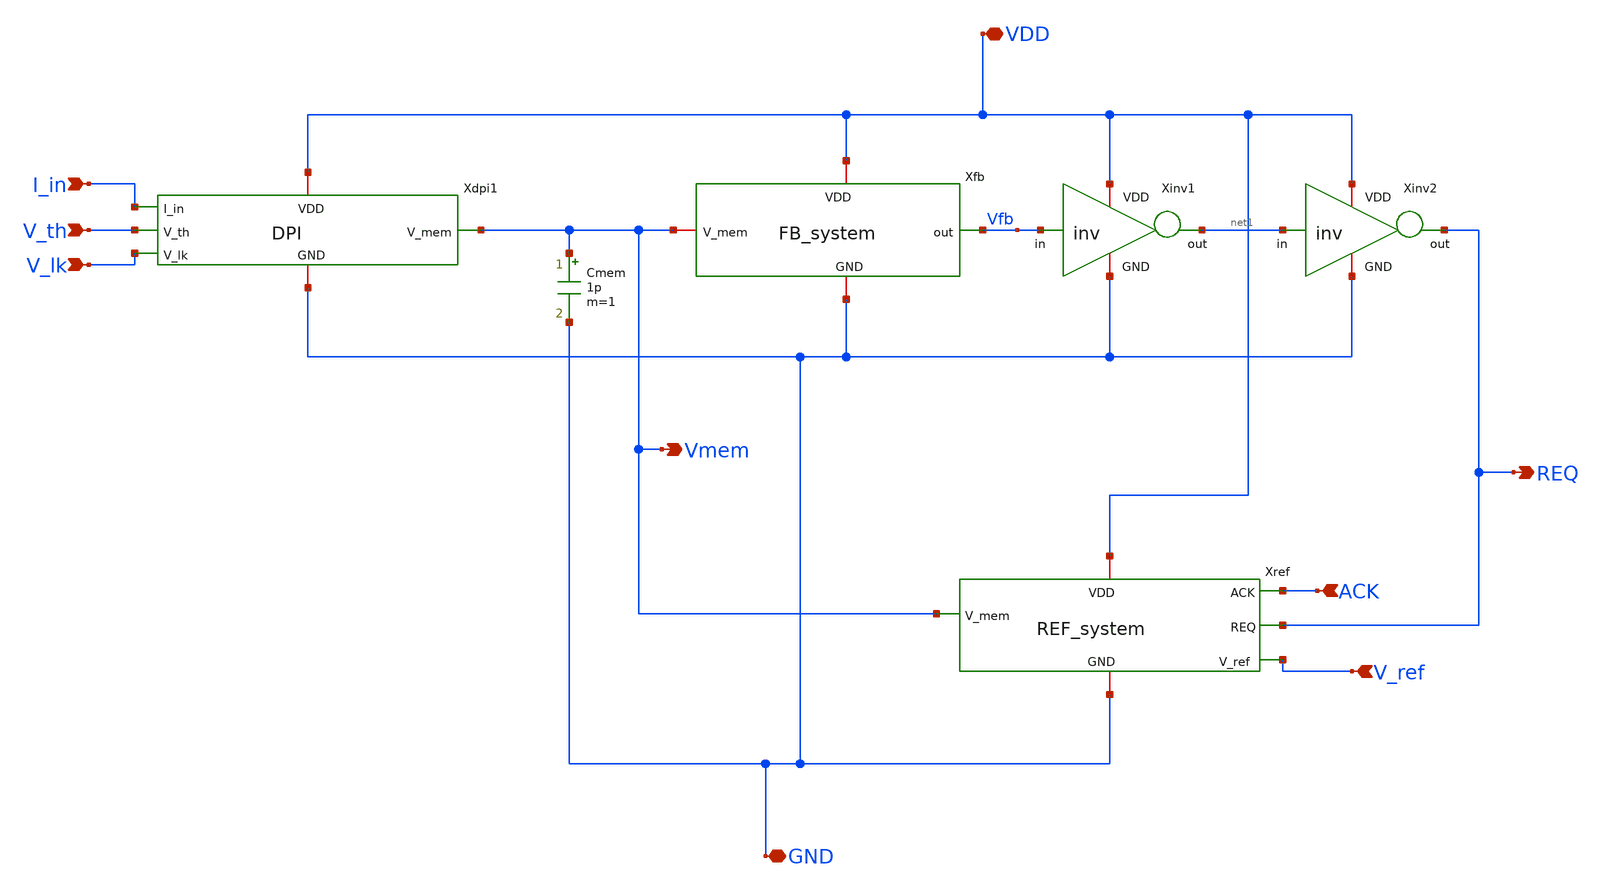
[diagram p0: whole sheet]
** sch_path: xschem/neuron_noahp.sch
**.subckt neuron_noahp V_ref GND VDD REQ ACK I_in V_th V_lk Vmem
*.ipin V_ref
*.iopin GND
*.iopin VDD
*.opin REQ
*.ipin ACK
*.ipin I_in
*.ipin V_th
*.ipin V_lk
*.opin Vmem
Xinv1 VDD Vfb net1 GND inv
Xinv2 VDD net1 REQ GND inv
Xdpi1 I_in VDD V_th Vmem V_lk GND DPI
Xfb VDD Vfb Vmem GND FB_system
Xref VDD ACK Vmem REQ V_ref GND REF_system
Cmem Vmem GND 1p m=1
**.ends

* expanding   symbol:  inv.sym # of pins=4
** sym_path: xschem/inv.sym
** sch_path: xschem/inv.sch
.subckt inv VDD in out GND
*.ipin in
*.iopin VDD
*.iopin GND
*.opin out
XM1 out in VDD VDD sg13_hv_pmos w=1u l=0.5u ng=1 m=1 mm_ok=1
XM2 out in GND GND sg13_hv_nmos w=1u l=0.5u ng=1 m=1 mm_ok=1
.ends


* expanding   symbol:  DPI.sym # of pins=6
** sym_path: xschem/DPI.sym
** sch_path: xschem/DPI.sch
.subckt DPI I_in VDD V_th V_mem V_lk GND
*.opin V_mem
*.ipin V_lk
*.ipin V_th
*.ipin I_in
*.iopin VDD
*.iopin GND
XMdifl GND V_th I_in VDD sg13_hv_pmos w=4u l=2u ng=2 m=8 mm_ok=1
XMdifr V_mem V_mem I_in VDD sg13_hv_pmos w=4u l=2u ng=2 m=8 mm_ok=1
XMtau net1 V_lk GND GND sg13_hv_nmos w=4u l=4u ng=2 m=4 mm_ok=1
Vilk V_mem net1 0
.save i(vilk)
.ends


* expanding   symbol:  FB_system.sym # of pins=4
** sym_path: FB_system.sym
** sch_path: FB_system.sch
.subckt FB_system VDD out V_mem GND
*.opin out
*.iopin V_mem
*.iopin VDD
*.iopin GND
XMmirr Vmir Vmir VDD VDD sg13_hv_pmos w=4u l=2u ng=4 m=1 mm_ok=1
XMfbsw V_mem out net1 VDD sg13_hv_pmos w=1u l=0.5u ng=2 m=1 mm_ok=1
XMmirl4 net1 Vmir net2 VDD sg13_hv_pmos w=1u l=2u ng=1 m=1 mm_ok=1
XMthr out V_mem Vmir VDD sg13_hv_pmos w=1u l=2u ng=2 m=4 mm_ok=1
XMmem1 out V_mem net3 GND sg13_hv_nmos w=1u l=2u ng=1 m=2 mm_ok=1
XMmirl3 net2 Vmir net4 VDD sg13_hv_pmos w=1u l=2u ng=1 m=1 mm_ok=1
XMmirl2 net4 Vmir net5 VDD sg13_hv_pmos w=1u l=2u ng=1 m=1 mm_ok=1
XMmirl1 net5 Vmir VDD VDD sg13_hv_pmos w=1u l=2u ng=1 m=1 mm_ok=1
XMmem2 net3 V_mem net6 GND sg13_hv_nmos w=1u l=2u ng=1 m=2 mm_ok=1
XMmem3 net6 V_mem net7 GND sg13_hv_nmos w=1u l=2u ng=1 m=2 mm_ok=1
XMmem4 net7 V_mem GND GND sg13_hv_nmos w=1u l=2u ng=1 m=2 mm_ok=1
.ends


* expanding   symbol:  REF_system.sym # of pins=6
** sym_path: xschem/REF_system.sym
** sch_path: xschem/REF_system.sch
.subckt REF_system VDD ACK V_mem REQ V_ref GND
*.iopin VDD
*.iopin GND
*.ipin V_ref
*.ipin REQ
*.ipin ACK
*.ipin V_mem
Cr Vref GND 0.5p m=1
XM10 Vref REQ net2 VDD sg13_hv_pmos w=1u l=0.5u ng=1 m=1 mm_ok=1
XM11 Vref REQ net1 GND sg13_hv_nmos w=1u l=0.5u ng=1 m=1 mm_ok=1
XM12 net2 ACK VDD VDD sg13_hv_pmos w=1u l=0.5u ng=1 m=1 mm_ok=1
XM13 V_mem Vref GND GND sg13_hv_nmos w=1u l=0.5u ng=1 m=1 mm_ok=1
XM14 net1 V_ref GND GND sg13_hv_nmos w=4u l=4u ng=2 m=4 mm_ok=1
.ends

.end
